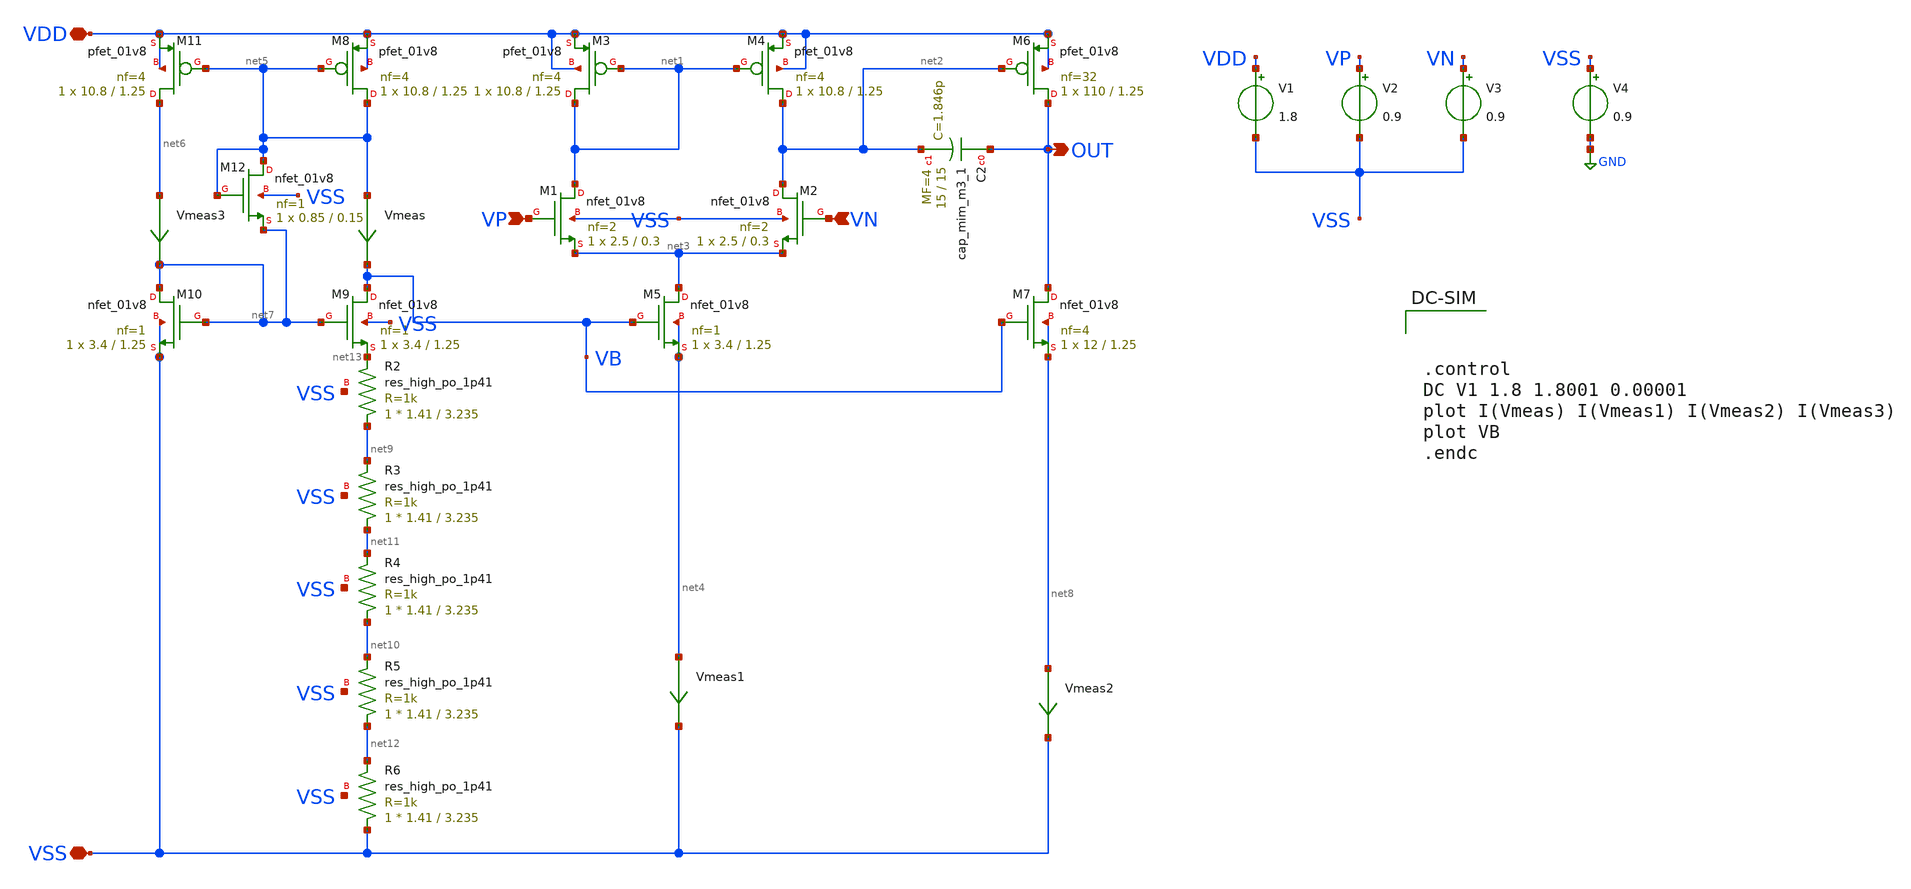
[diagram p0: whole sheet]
** sch_path: bandgap/tb_bgr-opamp/opamp-current.sch
**.subckt opamp-current VSS VDD VP VN OUT
*.iopin VSS
*.iopin VDD
*.ipin VP
*.ipin VN
*.opin OUT
XM1 net1 VP net3 VSS sky130_fd_pr__nfet_01v8 L=0.3 W=2.5 nf=2 ad='int((nf+1)/2) * W/nf * 0.29' as='int((nf+2)/2) * W/nf * 0.29'
+ pd='2*int((nf+1)/2) * (W/nf + 0.29)' ps='2*int((nf+2)/2) * (W/nf + 0.29)' nrd='0.29 / W' nrs='0.29 / W'
+ sa=0 sb=0 sd=0 mult=1 m=1
XM2 net2 VN net3 VSS sky130_fd_pr__nfet_01v8 L=0.3 W=2.5 nf=2 ad='int((nf+1)/2) * W/nf * 0.29' as='int((nf+2)/2) * W/nf * 0.29'
+ pd='2*int((nf+1)/2) * (W/nf + 0.29)' ps='2*int((nf+2)/2) * (W/nf + 0.29)' nrd='0.29 / W' nrs='0.29 / W'
+ sa=0 sb=0 sd=0 mult=1 m=1
XM4 net2 net1 VDD VDD sky130_fd_pr__pfet_01v8 L=1.25 W=10.8 nf=4 ad='int((nf+1)/2) * W/nf * 0.29' as='int((nf+2)/2) * W/nf * 0.29'
+ pd='2*int((nf+1)/2) * (W/nf + 0.29)' ps='2*int((nf+2)/2) * (W/nf + 0.29)' nrd='0.29 / W' nrs='0.29 / W'
+ sa=0 sb=0 sd=0 mult=1 m=1
XM3 net1 net1 VDD VDD sky130_fd_pr__pfet_01v8 L=1.25 W=10.8 nf=4 ad='int((nf+1)/2) * W/nf * 0.29' as='int((nf+2)/2) * W/nf * 0.29'
+ pd='2*int((nf+1)/2) * (W/nf + 0.29)' ps='2*int((nf+2)/2) * (W/nf + 0.29)' nrd='0.29 / W' nrs='0.29 / W'
+ sa=0 sb=0 sd=0 mult=1 m=1
XM5 net3 VB net4 net4 sky130_fd_pr__nfet_01v8 L=1.25 W=3.4 nf=1 ad='int((nf+1)/2) * W/nf * 0.29' as='int((nf+2)/2) * W/nf * 0.29'
+ pd='2*int((nf+1)/2) * (W/nf + 0.29)' ps='2*int((nf+2)/2) * (W/nf + 0.29)' nrd='0.29 / W' nrs='0.29 / W'
+ sa=0 sb=0 sd=0 mult=1 m=1
XM9 VB net7 net13 VSS sky130_fd_pr__nfet_01v8 L=1.25 W=3.4 nf=1 ad='int((nf+1)/2) * W/nf * 0.29' as='int((nf+2)/2) * W/nf * 0.29'
+ pd='2*int((nf+1)/2) * (W/nf + 0.29)' ps='2*int((nf+2)/2) * (W/nf + 0.29)' nrd='0.29 / W' nrs='0.29 / W'
+ sa=0 sb=0 sd=0 mult=1 m=1
XM8 net5 net5 VDD VDD sky130_fd_pr__pfet_01v8 L=1.25 W=10.8 nf=4 ad='int((nf+1)/2) * W/nf * 0.29' as='int((nf+2)/2) * W/nf * 0.29'
+ pd='2*int((nf+1)/2) * (W/nf + 0.29)' ps='2*int((nf+2)/2) * (W/nf + 0.29)' nrd='0.29 / W' nrs='0.29 / W'
+ sa=0 sb=0 sd=0 mult=1 m=1
XM11 net6 net5 VDD VDD sky130_fd_pr__pfet_01v8 L=1.25 W=10.8 nf=4 ad='int((nf+1)/2) * W/nf * 0.29' as='int((nf+2)/2) * W/nf * 0.29'
+ pd='2*int((nf+1)/2) * (W/nf + 0.29)' ps='2*int((nf+2)/2) * (W/nf + 0.29)' nrd='0.29 / W' nrs='0.29 / W'
+ sa=0 sb=0 sd=0 mult=1 m=1
XM10 net7 net7 VSS VSS sky130_fd_pr__nfet_01v8 L=1.25 W=3.4 nf=1 ad='int((nf+1)/2) * W/nf * 0.29' as='int((nf+2)/2) * W/nf * 0.29'
+ pd='2*int((nf+1)/2) * (W/nf + 0.29)' ps='2*int((nf+2)/2) * (W/nf + 0.29)' nrd='0.29 / W' nrs='0.29 / W'
+ sa=0 sb=0 sd=0 mult=1 m=1
XM6 OUT net2 VDD VDD sky130_fd_pr__pfet_01v8 L=1.25 W=110 nf=32 ad='int((nf+1)/2) * W/nf * 0.29' as='int((nf+2)/2) * W/nf * 0.29'
+ pd='2*int((nf+1)/2) * (W/nf + 0.29)' ps='2*int((nf+2)/2) * (W/nf + 0.29)' nrd='0.29 / W' nrs='0.29 / W'
+ sa=0 sb=0 sd=0 mult=1 m=1
XM7 OUT VB net8 net8 sky130_fd_pr__nfet_01v8 L=1.25 W=12 nf=4 ad='int((nf+1)/2) * W/nf * 0.29' as='int((nf+2)/2) * W/nf * 0.29'
+ pd='2*int((nf+1)/2) * (W/nf + 0.29)' ps='2*int((nf+2)/2) * (W/nf + 0.29)' nrd='0.29 / W' nrs='0.29 / W'
+ sa=0 sb=0 sd=0 mult=1 m=1
XC2 OUT net2 sky130_fd_pr__cap_mim_m3_1 W=15 L=15 MF=4 m=4
XM12 net5 net5 net7 VSS sky130_fd_pr__nfet_01v8 L=0.15 W=0.85 nf=1 ad='int((nf+1)/2) * W/nf * 0.29' as='int((nf+2)/2) * W/nf * 0.29'
+ pd='2*int((nf+1)/2) * (W/nf + 0.29)' ps='2*int((nf+2)/2) * (W/nf + 0.29)' nrd='0.29 / W' nrs='0.29 / W'
+ sa=0 sb=0 sd=0 mult=1 m=1
XR2 net9 net13 VSS sky130_fd_pr__res_high_po_1p41 L=3.235 mult=1 m=1
XR3 net11 net9 VSS sky130_fd_pr__res_high_po_1p41 L=3.235 mult=1 m=1
XR4 net10 net11 VSS sky130_fd_pr__res_high_po_1p41 L=3.235 mult=1 m=1
XR5 net12 net10 VSS sky130_fd_pr__res_high_po_1p41 L=3.235 mult=1 m=1
XR6 VSS net12 VSS sky130_fd_pr__res_high_po_1p41 L=3.235 mult=1 m=1
Vmeas net5 VB 0
.save i(vmeas)
Vmeas1 net4 VSS 0
.save i(vmeas1)
Vmeas2 net8 VSS 0
.save i(vmeas2)
V1 VDD VSS 1.8
V2 VP VSS 0.9
V3 VN VSS 0.9
V4 VSS GND 0.9
Vmeas3 net6 net7 0
.save i(vmeas3)
**** begin user architecture code

** opencircuitdesign pdks install
.lib $::SKYWATER_MODELS/sky130.lib.spice tt





.control
DC V1 1.8 1.8001 0.00001
plot I(Vmeas) I(Vmeas1) I(Vmeas2) I(Vmeas3)
plot VB
.endc



**** end user architecture code
**.ends
.GLOBAL GND
.end
